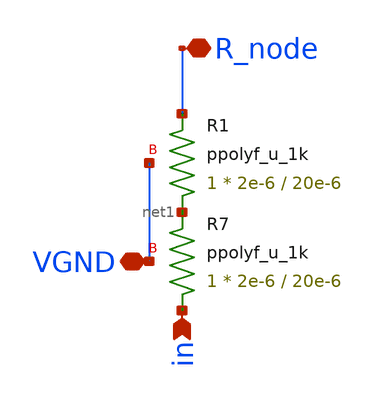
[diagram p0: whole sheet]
** sch_path: xschem/dac_sub_therm.sch
**.subckt dac_sub_therm in R_node VGND
*.ipin in
*.iopin R_node
*.iopin VGND
XR7 in net1 VGND ppolyf_u_1k r_width=2e-6 r_length=20e-6 m=1
XR1 net1 R_node VGND ppolyf_u_1k r_width=2e-6 r_length=20e-6 m=1
**.ends
.end
